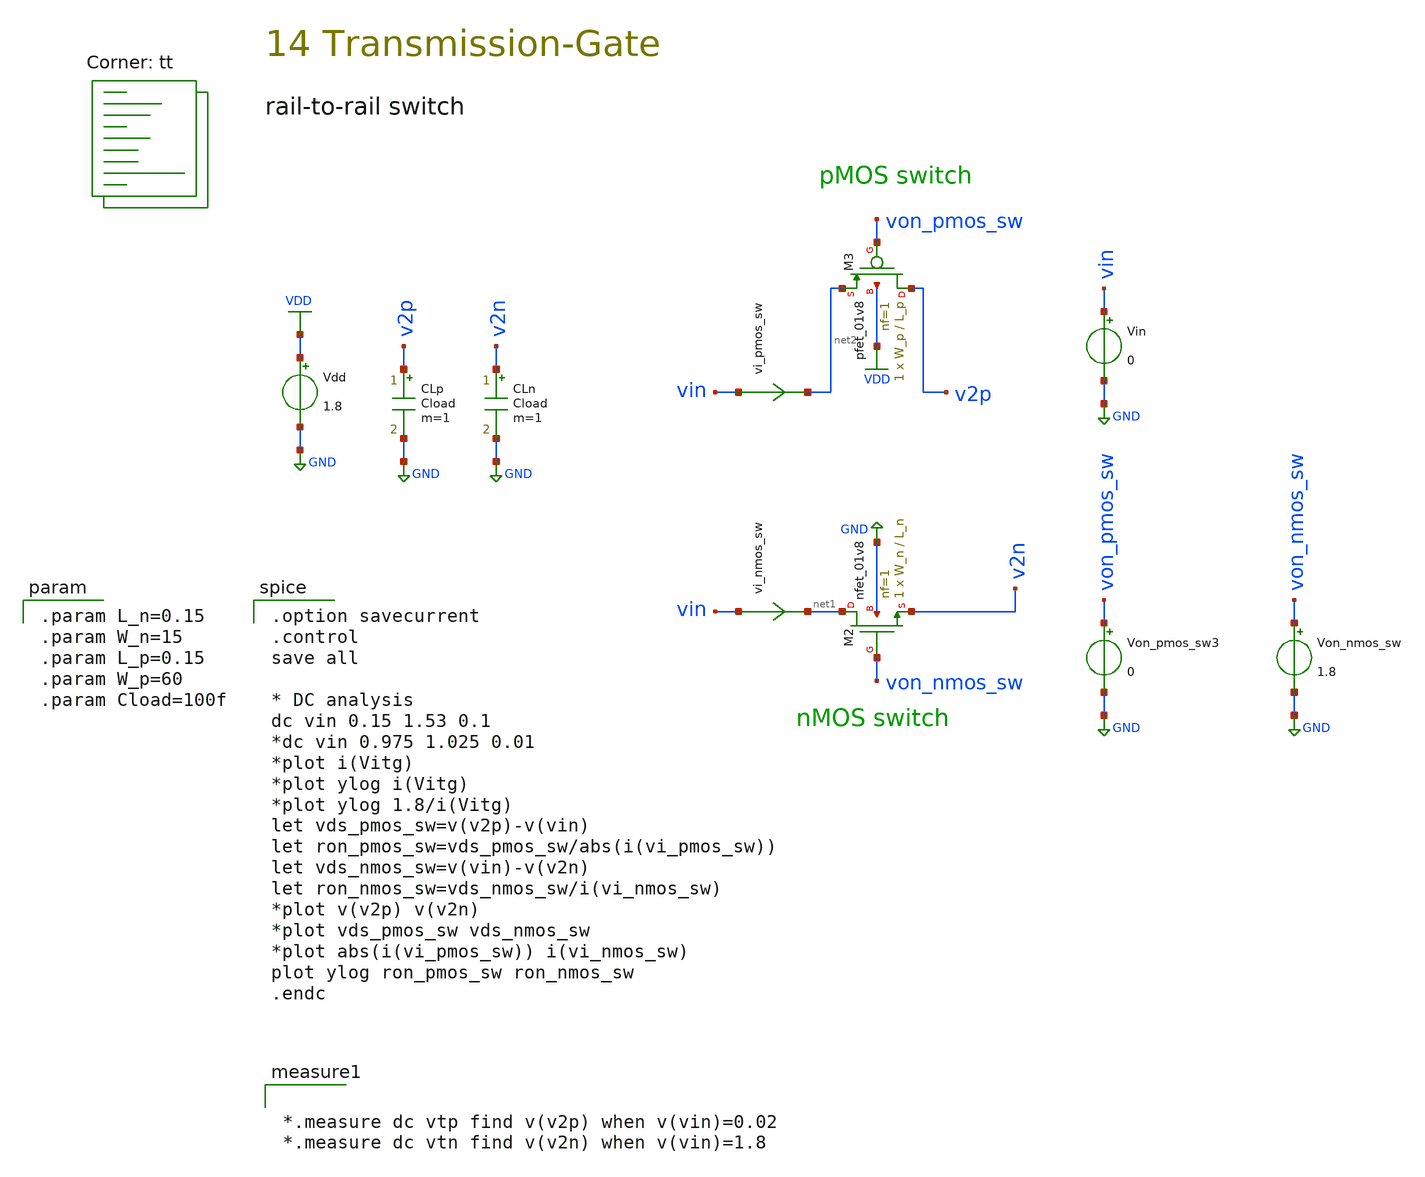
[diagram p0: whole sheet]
** sch_path: tseng_workspace/transmission_gate/schematic/spice/tg_dc_ron_eval.sch
**.subckt tg_dc_ron_eval
Vdd VDD GND 1.8
XM2 net1 von_nmos_sw v2n GND sky130_fd_pr__nfet_01v8 L=L_n W=W_n nf=1 ad='int((1 + 1)/2) * W_n / 1 * 0.29'
+ as='int((1 + 2)/2) * W_n / 1 * 0.29' pd='2*int((1 + 1)/2) * (W_n / 1 + 0.29)' ps='2*int((1 + 2)/2) * (W_n / 1 + 0.29)'
+ nrd='0.29 / W_n ' nrs='0.29 / W_n ' sa=0 sb=0 sd=0 mult=1 m=1
vi_nmos_sw vin net1 0
.save i(vi_nmos_sw)
Vin vin GND 0
Von_pmos_sw3 von_pmos_sw GND 0
Von_nmos_sw von_nmos_sw GND 1.8
XM3 v2p von_pmos_sw net2 VDD sky130_fd_pr__pfet_01v8 L=L_p W=W_p nf=1 ad='int((nf+1)/2) * W/nf * 0.29'
+ as='int((nf+2)/2) * W/nf * 0.29' pd='2*int((nf+1)/2) * (W/nf + 0.29)' ps='2*int((nf+2)/2) * (W/nf + 0.29)'
+ nrd='0.29 / W' nrs='0.29 / W' sa=0 sb=0 sd=0 mult=1 m=1
vi_pmos_sw vin net2 0
.save i(vi_pmos_sw)
CLp v2p GND Cload m=1
CLn v2n GND Cload m=1
**** begin user architecture code
.lib $::SKYWATER_MODELS/sky130.lib.spice tt

.option savecurrent
.control
save all

* DC analysis
dc vin 0.15 1.53 0.1
*dc vin 0.975 1.025 0.01
*plot i(Vitg)
*plot ylog i(Vitg)
*plot ylog 1.8/i(Vitg)
let vds_pmos_sw=v(v2p)-v(vin)
let ron_pmos_sw=vds_pmos_sw/abs(i(vi_pmos_sw))
let vds_nmos_sw=v(vin)-v(v2n)
let ron_nmos_sw=vds_nmos_sw/i(vi_nmos_sw)
*plot v(v2p) v(v2n)
*plot vds_pmos_sw vds_nmos_sw
*plot abs(i(vi_pmos_sw)) i(vi_nmos_sw)
plot ylog ron_pmos_sw ron_nmos_sw
.endc


.param L_n=0.15
.param W_n=15
.param L_p=0.15
.param W_p=60
.param Cload=100f


*.measure dc vtp find v(v2p) when v(vin)=0.02
*.measure dc vtn find v(v2n) when v(vin)=1.8

**** end user architecture code
**.ends
.GLOBAL GND
.GLOBAL VDD
.end
